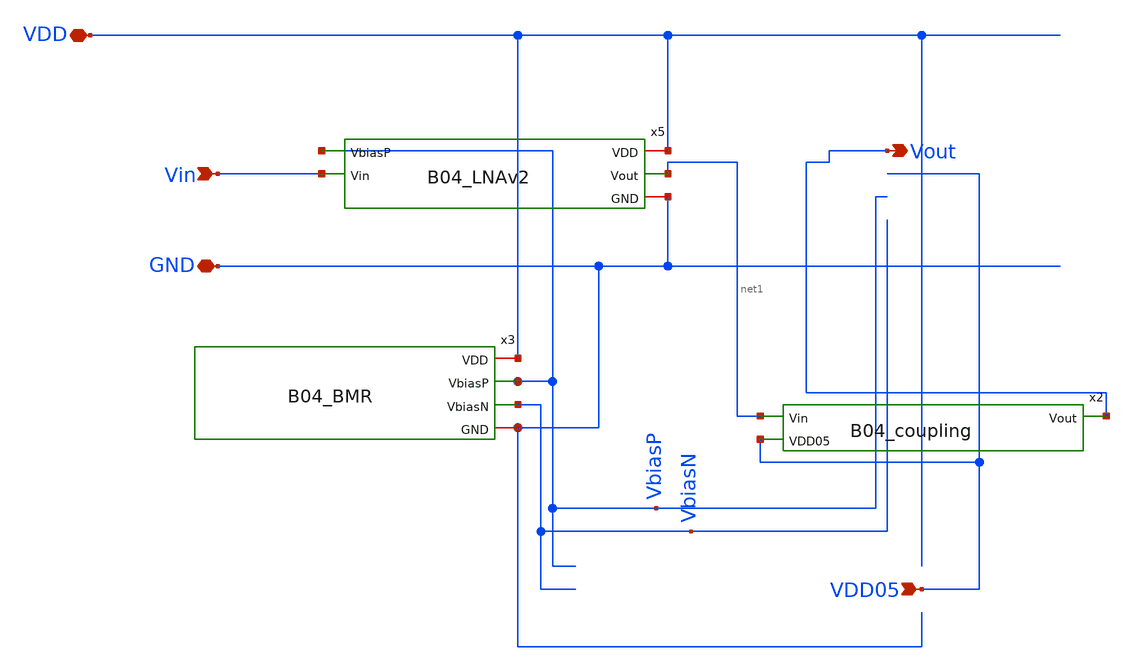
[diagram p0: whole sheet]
** sch_path: analog/B04_AFE.sch
**.subckt B04_AFE Vin VDD GND Vout VDD05
*.ipin Vin
*.iopin VDD
*.iopin GND
*.opin Vout
*.ipin VDD05
x5 VDD VbiasP net1 Vin GND B04_LNAv2
x3 VDD VbiasP VbiasN GND B04_BMR
x2 Vout net1 VDD05 B04_coupling
**.ends
.end
